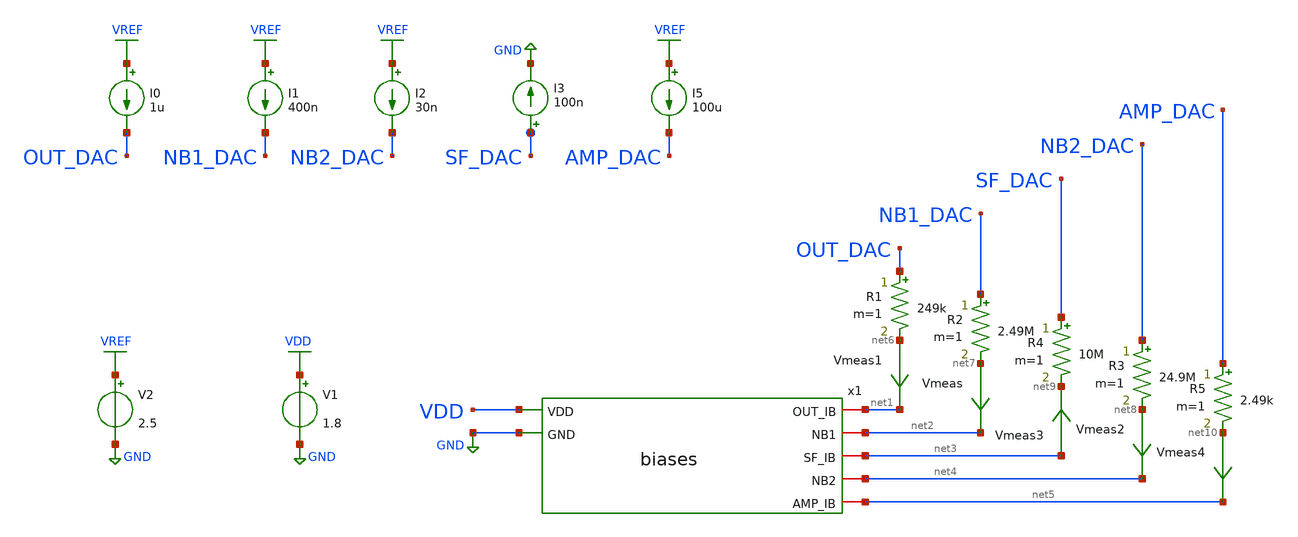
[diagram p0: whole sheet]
** sch_path: xschem/testbench/bias_board_tb.sch
**.subckt bias_board_tb
V1 VDD GND 1.8
x1 net1 VDD net2 GND net3 net4 net5 biases
R1 OUT_DAC net6 249k m=1
Vmeas net7 net2 0
.save i(vmeas)
Vmeas1 net6 net1 0
.save i(vmeas1)
Vmeas2 net8 net4 0
.save i(vmeas2)
Vmeas3 net3 net9 0
.save i(vmeas3)
Vmeas4 net10 net5 0
.save i(vmeas4)
R2 NB1_DAC net7 2.49M m=1
R3 NB2_DAC net8 24.9M m=1
R4 SF_DAC net9 10M m=1
R5 AMP_DAC net10 2.49k m=1
I0 VREF OUT_DAC 1u
I1 VREF NB1_DAC 400n
I2 VREF NB2_DAC 30n
I5 VREF AMP_DAC 100u
I3 SF_DAC GND 100n
V2 VREF GND 2.5
**** begin user architecture code

** opencircuitdesign pdks install
.lib $::SKYWATER_MODELS/sky130.lib.spice tt


**** end user architecture code
**.ends

* expanding   symbol:  biases.sym # of pins=7
** sym_path: xschem/biases.sym
** sch_path: xschem/biases.sch
.subckt biases OUT_IB VDD NB1 GND SF_IB NB2 AMP_IB
*.ipin VDD
*.ipin GND
*.iopin NB1
*.iopin NB2
*.iopin OUT_IB
*.iopin AMP_IB
*.iopin SF_IB
XM1 NB1 NB1 GND GND sky130_fd_pr__nfet_01v8_lvt L=1.2 W=1 nf=1 ad='int((nf+1)/2) * W/nf * 0.29' as='int((nf+2)/2) * W/nf * 0.29'
+ pd='2*int((nf+1)/2) * (W/nf + 0.29)' ps='2*int((nf+2)/2) * (W/nf + 0.29)' nrd='0.29 / W' nrs='0.29 / W'
+ sa=0 sb=0 sd=0 mult=1 m=1
XM3 NB2 NB2 GND GND sky130_fd_pr__nfet_01v8_lvt L=1.2 W=1 nf=1 ad='int((nf+1)/2) * W/nf * 0.29' as='int((nf+2)/2) * W/nf * 0.29'
+ pd='2*int((nf+1)/2) * (W/nf + 0.29)' ps='2*int((nf+2)/2) * (W/nf + 0.29)' nrd='0.29 / W' nrs='0.29 / W'
+ sa=0 sb=0 sd=0 mult=1 m=1
XM5 SF_IB SF_IB VDD VDD sky130_fd_pr__pfet_01v8_lvt L=1 W=1 nf=1 ad='int((nf+1)/2) * W/nf * 0.29' as='int((nf+2)/2) * W/nf * 0.29'
+ pd='2*int((nf+1)/2) * (W/nf + 0.29)' ps='2*int((nf+2)/2) * (W/nf + 0.29)' nrd='0.29 / W' nrs='0.29 / W'
+ sa=0 sb=0 sd=0 mult=1 m=1
XM4 OUT_IB OUT_IB GND GND sky130_fd_pr__nfet_01v8_lvt L=2 W=8 nf=1 ad='int((nf+1)/2) * W/nf * 0.29' as='int((nf+2)/2) * W/nf * 0.29'
+ pd='2*int((nf+1)/2) * (W/nf + 0.29)' ps='2*int((nf+2)/2) * (W/nf + 0.29)' nrd='0.29 / W' nrs='0.29 / W'
+ sa=0 sb=0 sd=0 mult=1 m=1
XM9 AMP_IB AMP_IB GND GND sky130_fd_pr__nfet_01v8_lvt L=2 W=8 nf=1 ad='int((nf+1)/2) * W/nf * 0.29' as='int((nf+2)/2) * W/nf * 0.29'
+ pd='2*int((nf+1)/2) * (W/nf + 0.29)' ps='2*int((nf+2)/2) * (W/nf + 0.29)' nrd='0.29 / W' nrs='0.29 / W'
+ sa=0 sb=0 sd=0 mult=1 m=1
.ends

.GLOBAL GND
.GLOBAL VDD
.GLOBAL VREF
**** begin user architecture code


.options gmin=0.0000000000000000000001
*.options savecurrents

.control
save all
op

.endc


**** end user architecture code
.end
